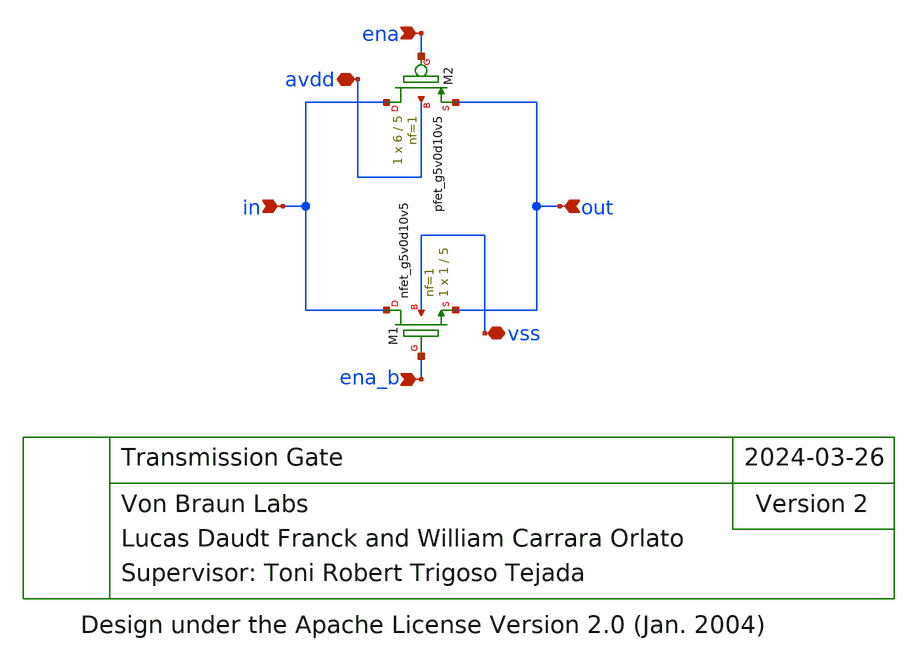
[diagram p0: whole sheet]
** sch_path: blocks/comp_hyst/xschem/trans_gate.sch
* Design under the Apache License Version 2.0 (Jan. 2004)
**.subckt trans_gate avdd vss ena ena_b in out
*.iopin avdd
*.iopin vss
*.ipin ena
*.ipin ena_b
*.ipin in
*.ipin out
XM1 in ena_b out vss sky130_fd_pr__nfet_g5v0d10v5 L=5 W=1 nf=1 ad='int((nf+1)/2) * W/nf * 0.29' as='int((nf+2)/2) * W/nf * 0.29'
+ pd='2*int((nf+1)/2) * (W/nf + 0.29)' ps='2*int((nf+2)/2) * (W/nf + 0.29)' nrd='0.29 / W' nrs='0.29 / W'
+ sa=0 sb=0 sd=0 mult=1 m=1
XM2 in ena out avdd sky130_fd_pr__pfet_g5v0d10v5 L=5 W=6 nf=1 ad='int((nf+1)/2) * W/nf * 0.29' as='int((nf+2)/2) * W/nf * 0.29'
+ pd='2*int((nf+1)/2) * (W/nf + 0.29)' ps='2*int((nf+2)/2) * (W/nf + 0.29)' nrd='0.29 / W' nrs='0.29 / W'
+ sa=0 sb=0 sd=0 mult=1 m=1
**.ends
.end
